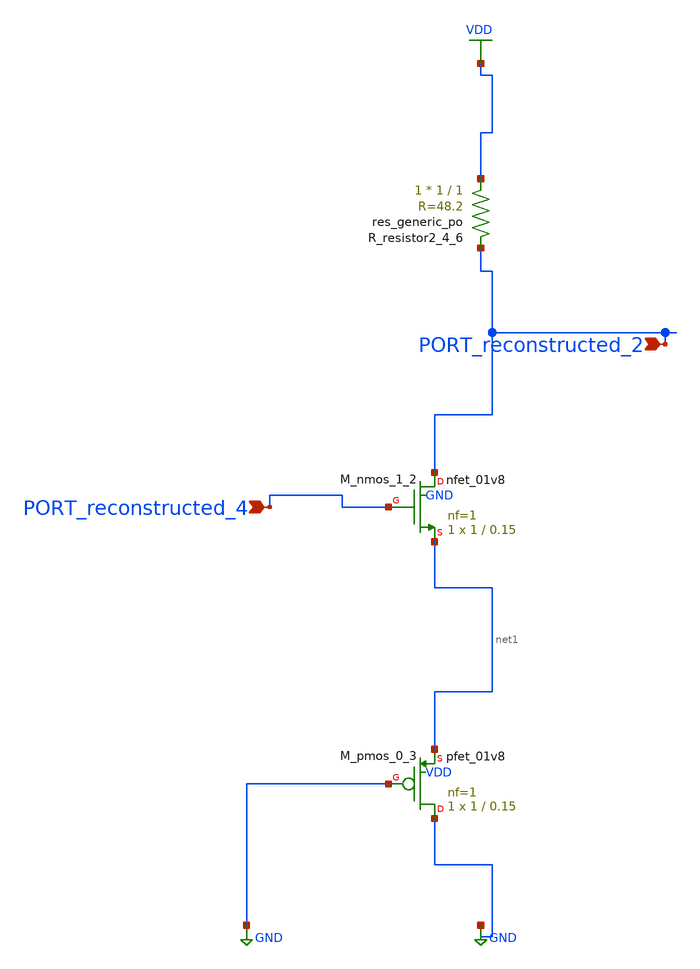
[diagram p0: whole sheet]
** sch_path: schematics/AMSNet/90.sch
**.subckt 90 PORT_reconstructed_2 PORT_reconstructed_4
*.ipin PORT_reconstructed_2
*.ipin PORT_reconstructed_4
XM_nmos_1_2 PORT_reconstructed_2 PORT_reconstructed_4 net1 GND sky130_fd_pr__nfet_01v8 L=0.15 W=1 nf=1
+ ad='int((1 + 1)/2) * 1 / 1 * 0.29' as='int((1 + 2)/2) * 1 / 1 * 0.29' pd='2*int((1 + 1)/2) * (1 / 1 + 0.29)'
+ ps='2*int((1 + 2)/2) * (1 / 1 + 0.29)' nrd='0.29 / 1 ' nrs='0.29 / 1 ' sa=0 sb=0 sd=0 mult=1 m=1
XM_pmos_0_3 GND GND net1 VDD sky130_fd_pr__pfet_01v8 L=0.15 W=1 nf=1 ad='int((1 + 1)/2) * 1 / 1 * 0.29'
+ as='int((1 + 2)/2) * 1 / 1 * 0.29' pd='2*int((1 + 1)/2) * (1 / 1 + 0.29)' ps='2*int((1 + 2)/2) * (1 / 1 + 0.29)'
+ nrd='0.29 / 1 ' nrs='0.29 / 1 ' sa=0 sb=0 sd=0 mult=1 m=1
XR_resistor2_4_6 VDD PORT_reconstructed_2 sky130_fd_pr__res_generic_po W=1 L=1 m=1
**.ends
.GLOBAL GND
.GLOBAL VDD
.end
